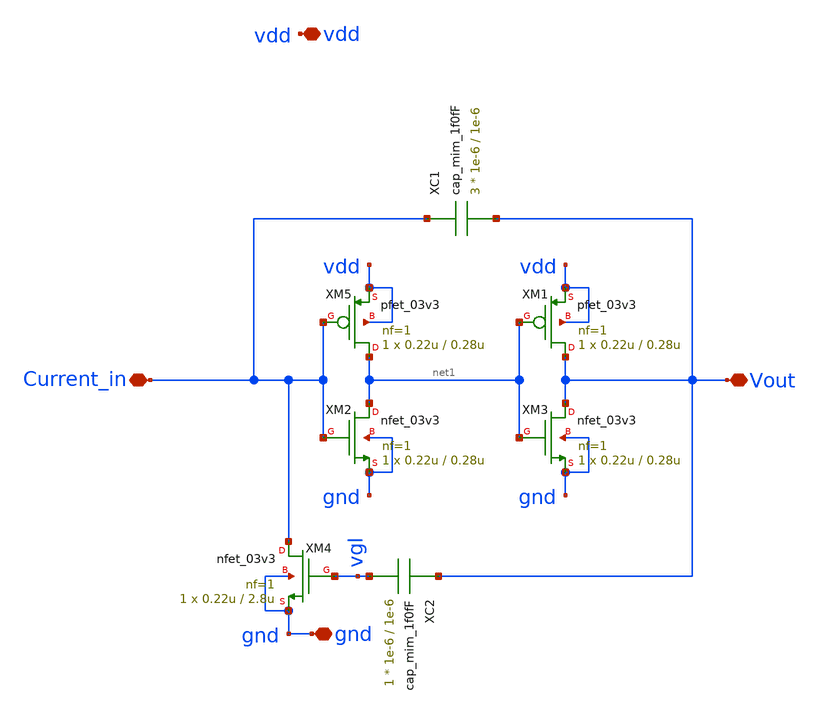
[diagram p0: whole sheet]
** sch_path: designs/libs/core_AH_neuron/AH_neuron.sch
**.subckt AH_neuron vdd gnd Current_in Vout
*.iopin vdd
*.iopin gnd
*.iopin Current_in
*.iopin Vout
XM5 net1 Current_in vdd vdd pfet_03v3 L=0.28u W=0.22u nf=1 ad='int((nf+1)/2) * W/nf * 0.18u' as='int((nf+2)/2) * W/nf * 0.18u'
+ pd='2*int((nf+1)/2) * (W/nf + 0.18u)' ps='2*int((nf+2)/2) * (W/nf + 0.18u)' nrd='0.18u / W' nrs='0.18u / W'
+ sa=0 sb=0 sd=0 m=1
XM1 Vout net1 vdd vdd pfet_03v3 L=0.28u W=0.22u nf=1 ad='int((nf+1)/2) * W/nf * 0.18u' as='int((nf+2)/2) * W/nf * 0.18u'
+ pd='2*int((nf+1)/2) * (W/nf + 0.18u)' ps='2*int((nf+2)/2) * (W/nf + 0.18u)' nrd='0.18u / W' nrs='0.18u / W'
+ sa=0 sb=0 sd=0 m=1
XM2 net1 Current_in gnd gnd nfet_03v3 L=0.28u W=0.22u nf=1 ad='int((nf+1)/2) * W/nf * 0.18u' as='int((nf+2)/2) * W/nf * 0.18u'
+ pd='2*int((nf+1)/2) * (W/nf + 0.18u)' ps='2*int((nf+2)/2) * (W/nf + 0.18u)' nrd='0.18u / W' nrs='0.18u / W'
+ sa=0 sb=0 sd=0 m=1
XM3 Vout net1 gnd gnd nfet_03v3 L=0.28u W=0.22u nf=1 ad='int((nf+1)/2) * W/nf * 0.18u' as='int((nf+2)/2) * W/nf * 0.18u'
+ pd='2*int((nf+1)/2) * (W/nf + 0.18u)' ps='2*int((nf+2)/2) * (W/nf + 0.18u)' nrd='0.18u / W' nrs='0.18u / W'
+ sa=0 sb=0 sd=0 m=1
XM4 Current_in vgl gnd gnd nfet_03v3 L=2.8u W=0.22u nf=1 ad='int((nf+1)/2) * W/nf * 0.18u' as='int((nf+2)/2) * W/nf * 0.18u'
+ pd='2*int((nf+1)/2) * (W/nf + 0.18u)' ps='2*int((nf+2)/2) * (W/nf + 0.18u)' nrd='0.18u / W' nrs='0.18u / W'
+ sa=0 sb=0 sd=0 m=1
XC1 Current_in Vout cap_mim_1f0fF c_width=1e-6 c_length=1e-6 m=3
XC2 Vout vgl cap_mim_1f0fF c_width=1e-6 c_length=1e-6 m=1
**.ends
.end
